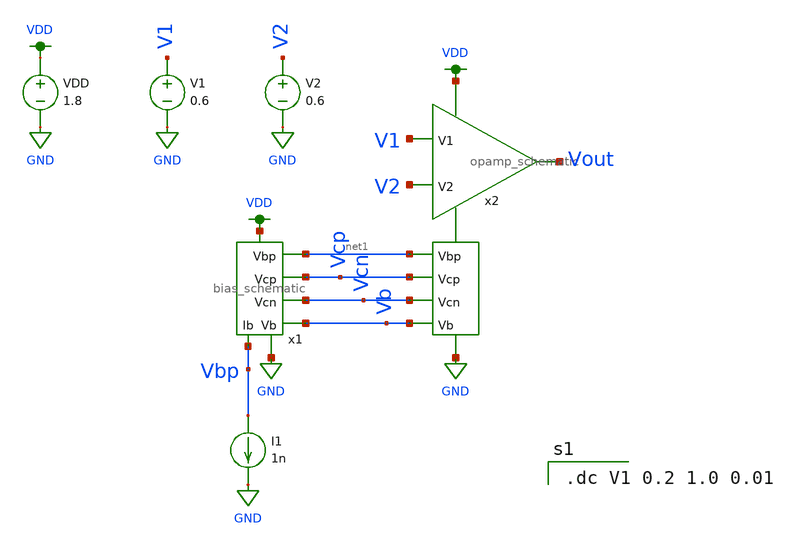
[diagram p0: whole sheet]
** sch_path: mp3/debug_files/test_opamp.sch
**.subckt test_opamp
x1 VDD net1 Vbp Vcp Vcn GND Vb bias_schematic
x2 VDD net1 Vcp Vout V1 V2 Vcn Vb GND opamp_schematic
I1 Vbp GND 1n
V1 V1 GND 0.6
V2 V2 GND 0.6
VDD VDD GND 1.8
**** begin user architecture code

.option wnflag=1
.lib ~/skywater/skywater-pdk/libraries/sky130_fd_pr_ngspice/latest/models/sky130.lib.spice tt


.dc V1 0.2 1.0 0.01

**** end user architecture code
**.ends

* expanding   symbol:  /home/madvlsi/dev/git/vlsi/mp3/xschem/bias_schematic.sym # of pins=7
** sym_path: mp3/debug_files/bias_schematic.sym
** sch_path: mp3/debug_files/bias_schematic.sch
.subckt bias_schematic VP Vbp Ib Vcp Vcn VN Vb
*.iopin VP
*.iopin VN
*.iopin Ib
*.opin Vcp
*.opin Vbp
*.opin Vcn
*.opin Vb
XM1a net2 net2 net1 GND sky130_fd_pr__nfet_01v8 L=0.5 W=30 nf=1 ad='int((nf+1)/2) * W/nf * 0.29' as='int((nf+2)/2) * W/nf * 0.29'
+ pd='2*int((nf+1)/2) * (W/nf + 0.29)' ps='2*int((nf+2)/2) * (W/nf + 0.29)' nrd='0.29 / W' nrs='0.29 / W'
+ sa=0 sb=0 sd=0 mult=1 m=1
XM1b net2 net2 net1 GND sky130_fd_pr__nfet_01v8 L=0.5 W=30 nf=1 ad='int((nf+1)/2) * W/nf * 0.29' as='int((nf+2)/2) * W/nf * 0.29'
+ pd='2*int((nf+1)/2) * (W/nf + 0.29)' ps='2*int((nf+2)/2) * (W/nf + 0.29)' nrd='0.29 / W' nrs='0.29 / W'
+ sa=0 sb=0 sd=0 mult=1 m=1
XM1c net2 net2 net1 GND sky130_fd_pr__nfet_01v8 L=0.5 W=30 nf=1 ad='int((nf+1)/2) * W/nf * 0.29' as='int((nf+2)/2) * W/nf * 0.29'
+ pd='2*int((nf+1)/2) * (W/nf + 0.29)' ps='2*int((nf+2)/2) * (W/nf + 0.29)' nrd='0.29 / W' nrs='0.29 / W'
+ sa=0 sb=0 sd=0 mult=1 m=1
XM1d net2 net2 net1 GND sky130_fd_pr__nfet_01v8 L=0.5 W=30 nf=1 ad='int((nf+1)/2) * W/nf * 0.29' as='int((nf+2)/2) * W/nf * 0.29'
+ pd='2*int((nf+1)/2) * (W/nf + 0.29)' ps='2*int((nf+2)/2) * (W/nf + 0.29)' nrd='0.29 / W' nrs='0.29 / W'
+ sa=0 sb=0 sd=0 mult=1 m=1
XM2a VN net2 net1 GND sky130_fd_pr__nfet_01v8 L=0.5 W=3 nf=1 ad='int((nf+1)/2) * W/nf * 0.29' as='int((nf+2)/2) * W/nf * 0.29'
+ pd='2*int((nf+1)/2) * (W/nf + 0.29)' ps='2*int((nf+2)/2) * (W/nf + 0.29)' nrd='0.29 / W' nrs='0.29 / W'
+ sa=0 sb=0 sd=0 mult=1 m=1
XM2b VN net2 net1 GND sky130_fd_pr__nfet_01v8 L=0.5 W=3 nf=1 ad='int((nf+1)/2) * W/nf * 0.29' as='int((nf+2)/2) * W/nf * 0.29'
+ pd='2*int((nf+1)/2) * (W/nf + 0.29)' ps='2*int((nf+2)/2) * (W/nf + 0.29)' nrd='0.29 / W' nrs='0.29 / W'
+ sa=0 sb=0 sd=0 mult=1 m=1
XM2c VN net2 net1 GND sky130_fd_pr__nfet_01v8 L=0.5 W=3 nf=1 ad='int((nf+1)/2) * W/nf * 0.29' as='int((nf+2)/2) * W/nf * 0.29'
+ pd='2*int((nf+1)/2) * (W/nf + 0.29)' ps='2*int((nf+2)/2) * (W/nf + 0.29)' nrd='0.29 / W' nrs='0.29 / W'
+ sa=0 sb=0 sd=0 mult=1 m=1
XM2d VN net2 net1 GND sky130_fd_pr__nfet_01v8 L=0.5 W=3 nf=1 ad='int((nf+1)/2) * W/nf * 0.29' as='int((nf+2)/2) * W/nf * 0.29'
+ pd='2*int((nf+1)/2) * (W/nf + 0.29)' ps='2*int((nf+2)/2) * (W/nf + 0.29)' nrd='0.29 / W' nrs='0.29 / W'
+ sa=0 sb=0 sd=0 mult=1 m=1
XM3a net2 Ib VP VDD sky130_fd_pr__pfet_01v8 L=0.5 W=3 nf=1 ad='int((nf+1)/2) * W/nf * 0.29' as='int((nf+2)/2) * W/nf * 0.29'
+ pd='2*int((nf+1)/2) * (W/nf + 0.29)' ps='2*int((nf+2)/2) * (W/nf + 0.29)' nrd='0.29 / W' nrs='0.29 / W'
+ sa=0 sb=0 sd=0 mult=1 m=1
XM3b net2 Ib VP VDD sky130_fd_pr__pfet_01v8 L=0.5 W=3 nf=1 ad='int((nf+1)/2) * W/nf * 0.29' as='int((nf+2)/2) * W/nf * 0.29'
+ pd='2*int((nf+1)/2) * (W/nf + 0.29)' ps='2*int((nf+2)/2) * (W/nf + 0.29)' nrd='0.29 / W' nrs='0.29 / W'
+ sa=0 sb=0 sd=0 mult=1 m=1
XM3c net2 Ib VP VDD sky130_fd_pr__pfet_01v8 L=0.5 W=3 nf=1 ad='int((nf+1)/2) * W/nf * 0.29' as='int((nf+2)/2) * W/nf * 0.29'
+ pd='2*int((nf+1)/2) * (W/nf + 0.29)' ps='2*int((nf+2)/2) * (W/nf + 0.29)' nrd='0.29 / W' nrs='0.29 / W'
+ sa=0 sb=0 sd=0 mult=1 m=1
XM3d net2 Ib VP VDD sky130_fd_pr__pfet_01v8 L=0.5 W=3 nf=1 ad='int((nf+1)/2) * W/nf * 0.29' as='int((nf+2)/2) * W/nf * 0.29'
+ pd='2*int((nf+1)/2) * (W/nf + 0.29)' ps='2*int((nf+2)/2) * (W/nf + 0.29)' nrd='0.29 / W' nrs='0.29 / W'
+ sa=0 sb=0 sd=0 mult=1 m=1
XM4a Vcn Ib VP VDD sky130_fd_pr__pfet_01v8 L=0.5 W=30 nf=1 ad='int((nf+1)/2) * W/nf * 0.29' as='int((nf+2)/2) * W/nf * 0.29'
+ pd='2*int((nf+1)/2) * (W/nf + 0.29)' ps='2*int((nf+2)/2) * (W/nf + 0.29)' nrd='0.29 / W' nrs='0.29 / W'
+ sa=0 sb=0 sd=0 mult=1 m=1
XM4b Vcn Ib VP VDD sky130_fd_pr__pfet_01v8 L=0.5 W=30 nf=1 ad='int((nf+1)/2) * W/nf * 0.29' as='int((nf+2)/2) * W/nf * 0.29'
+ pd='2*int((nf+1)/2) * (W/nf + 0.29)' ps='2*int((nf+2)/2) * (W/nf + 0.29)' nrd='0.29 / W' nrs='0.29 / W'
+ sa=0 sb=0 sd=0 mult=1 m=1
XM4c Vcn Ib VP VDD sky130_fd_pr__pfet_01v8 L=0.5 W=30 nf=1 ad='int((nf+1)/2) * W/nf * 0.29' as='int((nf+2)/2) * W/nf * 0.29'
+ pd='2*int((nf+1)/2) * (W/nf + 0.29)' ps='2*int((nf+2)/2) * (W/nf + 0.29)' nrd='0.29 / W' nrs='0.29 / W'
+ sa=0 sb=0 sd=0 mult=1 m=1
XM4d Vcn Ib VP VDD sky130_fd_pr__pfet_01v8 L=0.5 W=30 nf=1 ad='int((nf+1)/2) * W/nf * 0.29' as='int((nf+2)/2) * W/nf * 0.29'
+ pd='2*int((nf+1)/2) * (W/nf + 0.29)' ps='2*int((nf+2)/2) * (W/nf + 0.29)' nrd='0.29 / W' nrs='0.29 / W'
+ sa=0 sb=0 sd=0 mult=1 m=1
XM11a Ib Ib VP VDD sky130_fd_pr__pfet_01v8 L=0.5 W=3 nf=1 ad='int((nf+1)/2) * W/nf * 0.29' as='int((nf+2)/2) * W/nf * 0.29'
+ pd='2*int((nf+1)/2) * (W/nf + 0.29)' ps='2*int((nf+2)/2) * (W/nf + 0.29)' nrd='0.29 / W' nrs='0.29 / W'
+ sa=0 sb=0 sd=0 mult=1 m=1
XM11b Ib Ib VP VDD sky130_fd_pr__pfet_01v8 L=0.5 W=3 nf=1 ad='int((nf+1)/2) * W/nf * 0.29' as='int((nf+2)/2) * W/nf * 0.29'
+ pd='2*int((nf+1)/2) * (W/nf + 0.29)' ps='2*int((nf+2)/2) * (W/nf + 0.29)' nrd='0.29 / W' nrs='0.29 / W'
+ sa=0 sb=0 sd=0 mult=1 m=1
XM11c Ib Ib VP VDD sky130_fd_pr__pfet_01v8 L=0.5 W=3 nf=1 ad='int((nf+1)/2) * W/nf * 0.29' as='int((nf+2)/2) * W/nf * 0.29'
+ pd='2*int((nf+1)/2) * (W/nf + 0.29)' ps='2*int((nf+2)/2) * (W/nf + 0.29)' nrd='0.29 / W' nrs='0.29 / W'
+ sa=0 sb=0 sd=0 mult=1 m=1
XM11d Ib Ib VP VDD sky130_fd_pr__pfet_01v8 L=0.5 W=3 nf=1 ad='int((nf+1)/2) * W/nf * 0.29' as='int((nf+2)/2) * W/nf * 0.29'
+ pd='2*int((nf+1)/2) * (W/nf + 0.29)' ps='2*int((nf+2)/2) * (W/nf + 0.29)' nrd='0.29 / W' nrs='0.29 / W'
+ sa=0 sb=0 sd=0 mult=1 m=1
XM5a net1 Vcn Vcn GND sky130_fd_pr__nfet_01v8 L=0.5 W=30 nf=1 ad='int((nf+1)/2) * W/nf * 0.29' as='int((nf+2)/2) * W/nf * 0.29'
+ pd='2*int((nf+1)/2) * (W/nf + 0.29)' ps='2*int((nf+2)/2) * (W/nf + 0.29)' nrd='0.29 / W' nrs='0.29 / W'
+ sa=0 sb=0 sd=0 mult=1 m=1
XM5b net1 Vcn Vcn GND sky130_fd_pr__nfet_01v8 L=0.5 W=30 nf=1 ad='int((nf+1)/2) * W/nf * 0.29' as='int((nf+2)/2) * W/nf * 0.29'
+ pd='2*int((nf+1)/2) * (W/nf + 0.29)' ps='2*int((nf+2)/2) * (W/nf + 0.29)' nrd='0.29 / W' nrs='0.29 / W'
+ sa=0 sb=0 sd=0 mult=1 m=1
XM5c net1 Vcn Vcn GND sky130_fd_pr__nfet_01v8 L=0.5 W=30 nf=1 ad='int((nf+1)/2) * W/nf * 0.29' as='int((nf+2)/2) * W/nf * 0.29'
+ pd='2*int((nf+1)/2) * (W/nf + 0.29)' ps='2*int((nf+2)/2) * (W/nf + 0.29)' nrd='0.29 / W' nrs='0.29 / W'
+ sa=0 sb=0 sd=0 mult=1 m=1
XM5d net1 Vcn Vcn GND sky130_fd_pr__nfet_01v8 L=0.5 W=30 nf=1 ad='int((nf+1)/2) * W/nf * 0.29' as='int((nf+2)/2) * W/nf * 0.29'
+ pd='2*int((nf+1)/2) * (W/nf + 0.29)' ps='2*int((nf+2)/2) * (W/nf + 0.29)' nrd='0.29 / W' nrs='0.29 / W'
+ sa=0 sb=0 sd=0 mult=1 m=1
XM8a VN Vb net3 GND sky130_fd_pr__nfet_01v8 L=0.5 W=3 nf=1 ad='int((nf+1)/2) * W/nf * 0.29' as='int((nf+2)/2) * W/nf * 0.29'
+ pd='2*int((nf+1)/2) * (W/nf + 0.29)' ps='2*int((nf+2)/2) * (W/nf + 0.29)' nrd='0.29 / W' nrs='0.29 / W'
+ sa=0 sb=0 sd=0 mult=1 m=1
XM8b VN Vb net3 GND sky130_fd_pr__nfet_01v8 L=0.5 W=3 nf=1 ad='int((nf+1)/2) * W/nf * 0.29' as='int((nf+2)/2) * W/nf * 0.29'
+ pd='2*int((nf+1)/2) * (W/nf + 0.29)' ps='2*int((nf+2)/2) * (W/nf + 0.29)' nrd='0.29 / W' nrs='0.29 / W'
+ sa=0 sb=0 sd=0 mult=1 m=1
XM8c VN Vb net3 GND sky130_fd_pr__nfet_01v8 L=0.5 W=3 nf=1 ad='int((nf+1)/2) * W/nf * 0.29' as='int((nf+2)/2) * W/nf * 0.29'
+ pd='2*int((nf+1)/2) * (W/nf + 0.29)' ps='2*int((nf+2)/2) * (W/nf + 0.29)' nrd='0.29 / W' nrs='0.29 / W'
+ sa=0 sb=0 sd=0 mult=1 m=1
XM8d VN Vb net3 GND sky130_fd_pr__nfet_01v8 L=0.5 W=3 nf=1 ad='int((nf+1)/2) * W/nf * 0.29' as='int((nf+2)/2) * W/nf * 0.29'
+ pd='2*int((nf+1)/2) * (W/nf + 0.29)' ps='2*int((nf+2)/2) * (W/nf + 0.29)' nrd='0.29 / W' nrs='0.29 / W'
+ sa=0 sb=0 sd=0 mult=1 m=1
XM6a net3 net3 net4 VDD sky130_fd_pr__pfet_01v8 L=0.5 W=30 nf=1 ad='int((nf+1)/2) * W/nf * 0.29' as='int((nf+2)/2) * W/nf * 0.29'
+ pd='2*int((nf+1)/2) * (W/nf + 0.29)' ps='2*int((nf+2)/2) * (W/nf + 0.29)' nrd='0.29 / W' nrs='0.29 / W'
+ sa=0 sb=0 sd=0 mult=1 m=1
XM6b net3 net3 net4 VDD sky130_fd_pr__pfet_01v8 L=0.5 W=30 nf=1 ad='int((nf+1)/2) * W/nf * 0.29' as='int((nf+2)/2) * W/nf * 0.29'
+ pd='2*int((nf+1)/2) * (W/nf + 0.29)' ps='2*int((nf+2)/2) * (W/nf + 0.29)' nrd='0.29 / W' nrs='0.29 / W'
+ sa=0 sb=0 sd=0 mult=1 m=1
XM6c net3 net3 net4 VDD sky130_fd_pr__pfet_01v8 L=0.5 W=30 nf=1 ad='int((nf+1)/2) * W/nf * 0.29' as='int((nf+2)/2) * W/nf * 0.29'
+ pd='2*int((nf+1)/2) * (W/nf + 0.29)' ps='2*int((nf+2)/2) * (W/nf + 0.29)' nrd='0.29 / W' nrs='0.29 / W'
+ sa=0 sb=0 sd=0 mult=1 m=1
XM6d net3 net3 net4 VDD sky130_fd_pr__pfet_01v8 L=0.5 W=30 nf=1 ad='int((nf+1)/2) * W/nf * 0.29' as='int((nf+2)/2) * W/nf * 0.29'
+ pd='2*int((nf+1)/2) * (W/nf + 0.29)' ps='2*int((nf+2)/2) * (W/nf + 0.29)' nrd='0.29 / W' nrs='0.29 / W'
+ sa=0 sb=0 sd=0 mult=1 m=1
XM7a net4 net3 VP VDD sky130_fd_pr__pfet_01v8 L=0.5 W=3 nf=1 ad='int((nf+1)/2) * W/nf * 0.29' as='int((nf+2)/2) * W/nf * 0.29'
+ pd='2*int((nf+1)/2) * (W/nf + 0.29)' ps='2*int((nf+2)/2) * (W/nf + 0.29)' nrd='0.29 / W' nrs='0.29 / W'
+ sa=0 sb=0 sd=0 mult=1 m=1
XM7b net4 net3 VP VDD sky130_fd_pr__pfet_01v8 L=0.5 W=3 nf=1 ad='int((nf+1)/2) * W/nf * 0.29' as='int((nf+2)/2) * W/nf * 0.29'
+ pd='2*int((nf+1)/2) * (W/nf + 0.29)' ps='2*int((nf+2)/2) * (W/nf + 0.29)' nrd='0.29 / W' nrs='0.29 / W'
+ sa=0 sb=0 sd=0 mult=1 m=1
XM7c net4 net3 VP VDD sky130_fd_pr__pfet_01v8 L=0.5 W=3 nf=1 ad='int((nf+1)/2) * W/nf * 0.29' as='int((nf+2)/2) * W/nf * 0.29'
+ pd='2*int((nf+1)/2) * (W/nf + 0.29)' ps='2*int((nf+2)/2) * (W/nf + 0.29)' nrd='0.29 / W' nrs='0.29 / W'
+ sa=0 sb=0 sd=0 mult=1 m=1
XM7d net4 net3 VP VDD sky130_fd_pr__pfet_01v8 L=0.5 W=3 nf=1 ad='int((nf+1)/2) * W/nf * 0.29' as='int((nf+2)/2) * W/nf * 0.29'
+ pd='2*int((nf+1)/2) * (W/nf + 0.29)' ps='2*int((nf+2)/2) * (W/nf + 0.29)' nrd='0.29 / W' nrs='0.29 / W'
+ sa=0 sb=0 sd=0 mult=1 m=1
XM10d net4 Vcp Vcp VDD sky130_fd_pr__pfet_01v8 L=0.5 W=30 nf=1 ad='int((nf+1)/2) * W/nf * 0.29' as='int((nf+2)/2) * W/nf * 0.29'
+ pd='2*int((nf+1)/2) * (W/nf + 0.29)' ps='2*int((nf+2)/2) * (W/nf + 0.29)' nrd='0.29 / W' nrs='0.29 / W'
+ sa=0 sb=0 sd=0 mult=1 m=1
XM10c net4 Vcp Vcp VDD sky130_fd_pr__pfet_01v8 L=0.5 W=30 nf=1 ad='int((nf+1)/2) * W/nf * 0.29' as='int((nf+2)/2) * W/nf * 0.29'
+ pd='2*int((nf+1)/2) * (W/nf + 0.29)' ps='2*int((nf+2)/2) * (W/nf + 0.29)' nrd='0.29 / W' nrs='0.29 / W'
+ sa=0 sb=0 sd=0 mult=1 m=1
XM10b net4 Vcp Vcp VDD sky130_fd_pr__pfet_01v8 L=0.5 W=30 nf=1 ad='int((nf+1)/2) * W/nf * 0.29' as='int((nf+2)/2) * W/nf * 0.29'
+ pd='2*int((nf+1)/2) * (W/nf + 0.29)' ps='2*int((nf+2)/2) * (W/nf + 0.29)' nrd='0.29 / W' nrs='0.29 / W'
+ sa=0 sb=0 sd=0 mult=1 m=1
XM10a net4 Vcp Vcp VDD sky130_fd_pr__pfet_01v8 L=0.5 W=30 nf=1 ad='int((nf+1)/2) * W/nf * 0.29' as='int((nf+2)/2) * W/nf * 0.29'
+ pd='2*int((nf+1)/2) * (W/nf + 0.29)' ps='2*int((nf+2)/2) * (W/nf + 0.29)' nrd='0.29 / W' nrs='0.29 / W'
+ sa=0 sb=0 sd=0 mult=1 m=1
XM9a VN Vb Vcp GND sky130_fd_pr__nfet_01v8 L=0.5 W=30 nf=1 ad='int((nf+1)/2) * W/nf * 0.29' as='int((nf+2)/2) * W/nf * 0.29'
+ pd='2*int((nf+1)/2) * (W/nf + 0.29)' ps='2*int((nf+2)/2) * (W/nf + 0.29)' nrd='0.29 / W' nrs='0.29 / W'
+ sa=0 sb=0 sd=0 mult=1 m=1
XM9b VN Vb Vcp GND sky130_fd_pr__nfet_01v8 L=0.5 W=30 nf=1 ad='int((nf+1)/2) * W/nf * 0.29' as='int((nf+2)/2) * W/nf * 0.29'
+ pd='2*int((nf+1)/2) * (W/nf + 0.29)' ps='2*int((nf+2)/2) * (W/nf + 0.29)' nrd='0.29 / W' nrs='0.29 / W'
+ sa=0 sb=0 sd=0 mult=1 m=1
XM9c VN Vb Vcp GND sky130_fd_pr__nfet_01v8 L=0.5 W=30 nf=1 ad='int((nf+1)/2) * W/nf * 0.29' as='int((nf+2)/2) * W/nf * 0.29'
+ pd='2*int((nf+1)/2) * (W/nf + 0.29)' ps='2*int((nf+2)/2) * (W/nf + 0.29)' nrd='0.29 / W' nrs='0.29 / W'
+ sa=0 sb=0 sd=0 mult=1 m=1
XM9d VN Vb Vcp GND sky130_fd_pr__nfet_01v8 L=0.5 W=30 nf=1 ad='int((nf+1)/2) * W/nf * 0.29' as='int((nf+2)/2) * W/nf * 0.29'
+ pd='2*int((nf+1)/2) * (W/nf + 0.29)' ps='2*int((nf+2)/2) * (W/nf + 0.29)' nrd='0.29 / W' nrs='0.29 / W'
+ sa=0 sb=0 sd=0 mult=1 m=1
XM12a VN Vb Vb GND sky130_fd_pr__nfet_01v8 L=0.5 W=3 nf=1 ad='int((nf+1)/2) * W/nf * 0.29' as='int((nf+2)/2) * W/nf * 0.29'
+ pd='2*int((nf+1)/2) * (W/nf + 0.29)' ps='2*int((nf+2)/2) * (W/nf + 0.29)' nrd='0.29 / W' nrs='0.29 / W'
+ sa=0 sb=0 sd=0 mult=1 m=1
XM12b VN Vb Vb GND sky130_fd_pr__nfet_01v8 L=0.5 W=3 nf=1 ad='int((nf+1)/2) * W/nf * 0.29' as='int((nf+2)/2) * W/nf * 0.29'
+ pd='2*int((nf+1)/2) * (W/nf + 0.29)' ps='2*int((nf+2)/2) * (W/nf + 0.29)' nrd='0.29 / W' nrs='0.29 / W'
+ sa=0 sb=0 sd=0 mult=1 m=1
XM12c VN Vb Vb GND sky130_fd_pr__nfet_01v8 L=0.5 W=3 nf=1 ad='int((nf+1)/2) * W/nf * 0.29' as='int((nf+2)/2) * W/nf * 0.29'
+ pd='2*int((nf+1)/2) * (W/nf + 0.29)' ps='2*int((nf+2)/2) * (W/nf + 0.29)' nrd='0.29 / W' nrs='0.29 / W'
+ sa=0 sb=0 sd=0 mult=1 m=1
XM12d VN Vb Vb GND sky130_fd_pr__nfet_01v8 L=0.5 W=3 nf=1 ad='int((nf+1)/2) * W/nf * 0.29' as='int((nf+2)/2) * W/nf * 0.29'
+ pd='2*int((nf+1)/2) * (W/nf + 0.29)' ps='2*int((nf+2)/2) * (W/nf + 0.29)' nrd='0.29 / W' nrs='0.29 / W'
+ sa=0 sb=0 sd=0 mult=1 m=1
XM1 Vb Ib VP VDD sky130_fd_pr__pfet_01v8 L=0.5 W=3 nf=1 ad='int((nf+1)/2) * W/nf * 0.29' as='int((nf+2)/2) * W/nf * 0.29'
+ pd='2*int((nf+1)/2) * (W/nf + 0.29)' ps='2*int((nf+2)/2) * (W/nf + 0.29)' nrd='0.29 / W' nrs='0.29 / W'
+ sa=0 sb=0 sd=0 mult=1 m=1
XM2 Vb Ib VP VDD sky130_fd_pr__pfet_01v8 L=0.5 W=3 nf=1 ad='int((nf+1)/2) * W/nf * 0.29' as='int((nf+2)/2) * W/nf * 0.29'
+ pd='2*int((nf+1)/2) * (W/nf + 0.29)' ps='2*int((nf+2)/2) * (W/nf + 0.29)' nrd='0.29 / W' nrs='0.29 / W'
+ sa=0 sb=0 sd=0 mult=1 m=1
XM3 Vb Ib VP VDD sky130_fd_pr__pfet_01v8 L=0.5 W=3 nf=1 ad='int((nf+1)/2) * W/nf * 0.29' as='int((nf+2)/2) * W/nf * 0.29'
+ pd='2*int((nf+1)/2) * (W/nf + 0.29)' ps='2*int((nf+2)/2) * (W/nf + 0.29)' nrd='0.29 / W' nrs='0.29 / W'
+ sa=0 sb=0 sd=0 mult=1 m=1
XM4 Vb Ib VP VDD sky130_fd_pr__pfet_01v8 L=0.5 W=3 nf=1 ad='int((nf+1)/2) * W/nf * 0.29' as='int((nf+2)/2) * W/nf * 0.29'
+ pd='2*int((nf+1)/2) * (W/nf + 0.29)' ps='2*int((nf+2)/2) * (W/nf + 0.29)' nrd='0.29 / W' nrs='0.29 / W'
+ sa=0 sb=0 sd=0 mult=1 m=1
.ends


* expanding   symbol:  /home/madvlsi/dev/git/vlsi/mp3/xschem/opamp_schematic.sym # of pins=9
** sym_path: /home/madvlsi/dev/git/vlsi/mp3/xschem/opamp_schematic.sym
** sch_path: /home/madvlsi/dev/git/vlsi/mp3/xschem/opamp_schematic.sch
.subckt opamp_schematic VP Vbp Vcp Vout V1 V2 Vcn Vb VN
*.ipin Vbp
*.ipin Vcp
*.ipin Vcn
*.ipin V2
*.ipin V1
*.ipin Vb
*.iopin VP
*.iopin VN
*.opin Vout
XM1a M1top V1 Vnode GND sky130_fd_pr__nfet_01v8 L=0.5 W=3 nf=1 ad='int((nf+1)/2) * W/nf * 0.29' as='int((nf+2)/2) * W/nf * 0.29'
+ pd='2*int((nf+1)/2) * (W/nf + 0.29)' ps='2*int((nf+2)/2) * (W/nf + 0.29)' nrd='0.29 / W' nrs='0.29 / W'
+ sa=0 sb=0 sd=0 mult=1 m=1
XM1b M1top V1 Vnode GND sky130_fd_pr__nfet_01v8 L=0.5 W=3 nf=1 ad='int((nf+1)/2) * W/nf * 0.29' as='int((nf+2)/2) * W/nf * 0.29'
+ pd='2*int((nf+1)/2) * (W/nf + 0.29)' ps='2*int((nf+2)/2) * (W/nf + 0.29)' nrd='0.29 / W' nrs='0.29 / W'
+ sa=0 sb=0 sd=0 mult=1 m=1
XM1c M1top V1 Vnode GND sky130_fd_pr__nfet_01v8 L=0.5 W=3 nf=1 ad='int((nf+1)/2) * W/nf * 0.29' as='int((nf+2)/2) * W/nf * 0.29'
+ pd='2*int((nf+1)/2) * (W/nf + 0.29)' ps='2*int((nf+2)/2) * (W/nf + 0.29)' nrd='0.29 / W' nrs='0.29 / W'
+ sa=0 sb=0 sd=0 mult=1 m=1
XM1d M1top V1 Vnode GND sky130_fd_pr__nfet_01v8 L=0.5 W=3 nf=1 ad='int((nf+1)/2) * W/nf * 0.29' as='int((nf+2)/2) * W/nf * 0.29'
+ pd='2*int((nf+1)/2) * (W/nf + 0.29)' ps='2*int((nf+2)/2) * (W/nf + 0.29)' nrd='0.29 / W' nrs='0.29 / W'
+ sa=0 sb=0 sd=0 mult=1 m=1
XM2a M2top V2 Vnode GND sky130_fd_pr__nfet_01v8 L=0.5 W=3 nf=1 ad='int((nf+1)/2) * W/nf * 0.29' as='int((nf+2)/2) * W/nf * 0.29'
+ pd='2*int((nf+1)/2) * (W/nf + 0.29)' ps='2*int((nf+2)/2) * (W/nf + 0.29)' nrd='0.29 / W' nrs='0.29 / W'
+ sa=0 sb=0 sd=0 mult=1 m=1
XM2b M2top V2 Vnode GND sky130_fd_pr__nfet_01v8 L=0.5 W=3 nf=1 ad='int((nf+1)/2) * W/nf * 0.29' as='int((nf+2)/2) * W/nf * 0.29'
+ pd='2*int((nf+1)/2) * (W/nf + 0.29)' ps='2*int((nf+2)/2) * (W/nf + 0.29)' nrd='0.29 / W' nrs='0.29 / W'
+ sa=0 sb=0 sd=0 mult=1 m=1
XM2c M2top V2 Vnode GND sky130_fd_pr__nfet_01v8 L=0.5 W=3 nf=1 ad='int((nf+1)/2) * W/nf * 0.29' as='int((nf+2)/2) * W/nf * 0.29'
+ pd='2*int((nf+1)/2) * (W/nf + 0.29)' ps='2*int((nf+2)/2) * (W/nf + 0.29)' nrd='0.29 / W' nrs='0.29 / W'
+ sa=0 sb=0 sd=0 mult=1 m=1
XM2d M2top V2 Vnode GND sky130_fd_pr__nfet_01v8 L=0.5 W=3 nf=1 ad='int((nf+1)/2) * W/nf * 0.29' as='int((nf+2)/2) * W/nf * 0.29'
+ pd='2*int((nf+1)/2) * (W/nf + 0.29)' ps='2*int((nf+2)/2) * (W/nf + 0.29)' nrd='0.29 / W' nrs='0.29 / W'
+ sa=0 sb=0 sd=0 mult=1 m=1
XMba Vnode Vb VN GND sky130_fd_pr__nfet_01v8 L=0.5 W=1.5 nf=1 ad='int((nf+1)/2) * W/nf * 0.29' as='int((nf+2)/2) * W/nf * 0.29'
+ pd='2*int((nf+1)/2) * (W/nf + 0.29)' ps='2*int((nf+2)/2) * (W/nf + 0.29)' nrd='0.29 / W' nrs='0.29 / W'
+ sa=0 sb=0 sd=0 mult=1 m=1
XMbb Vnode Vb VN GND sky130_fd_pr__nfet_01v8 L=0.5 W=1.5 nf=1 ad='int((nf+1)/2) * W/nf * 0.29' as='int((nf+2)/2) * W/nf * 0.29'
+ pd='2*int((nf+1)/2) * (W/nf + 0.29)' ps='2*int((nf+2)/2) * (W/nf + 0.29)' nrd='0.29 / W' nrs='0.29 / W'
+ sa=0 sb=0 sd=0 mult=1 m=1
XMbc Vnode Vb VN GND sky130_fd_pr__nfet_01v8 L=0.5 W=1.5 nf=1 ad='int((nf+1)/2) * W/nf * 0.29' as='int((nf+2)/2) * W/nf * 0.29'
+ pd='2*int((nf+1)/2) * (W/nf + 0.29)' ps='2*int((nf+2)/2) * (W/nf + 0.29)' nrd='0.29 / W' nrs='0.29 / W'
+ sa=0 sb=0 sd=0 mult=1 m=1
XMbd Vnode Vb VN GND sky130_fd_pr__nfet_01v8 L=0.5 W=1.5 nf=1 ad='int((nf+1)/2) * W/nf * 0.29' as='int((nf+2)/2) * W/nf * 0.29'
+ pd='2*int((nf+1)/2) * (W/nf + 0.29)' ps='2*int((nf+2)/2) * (W/nf + 0.29)' nrd='0.29 / W' nrs='0.29 / W'
+ sa=0 sb=0 sd=0 mult=1 m=1
XMbe Vnode Vb VN GND sky130_fd_pr__nfet_01v8 L=0.5 W=1.5 nf=1 ad='int((nf+1)/2) * W/nf * 0.29' as='int((nf+2)/2) * W/nf * 0.29'
+ pd='2*int((nf+1)/2) * (W/nf + 0.29)' ps='2*int((nf+2)/2) * (W/nf + 0.29)' nrd='0.29 / W' nrs='0.29 / W'
+ sa=0 sb=0 sd=0 mult=1 m=1
XMbf Vnode Vb VN GND sky130_fd_pr__nfet_01v8 L=0.5 W=1.5 nf=1 ad='int((nf+1)/2) * W/nf * 0.29' as='int((nf+2)/2) * W/nf * 0.29'
+ pd='2*int((nf+1)/2) * (W/nf + 0.29)' ps='2*int((nf+2)/2) * (W/nf + 0.29)' nrd='0.29 / W' nrs='0.29 / W'
+ sa=0 sb=0 sd=0 mult=1 m=1
XMbg Vnode Vb VN GND sky130_fd_pr__nfet_01v8 L=0.5 W=1.5 nf=1 ad='int((nf+1)/2) * W/nf * 0.29' as='int((nf+2)/2) * W/nf * 0.29'
+ pd='2*int((nf+1)/2) * (W/nf + 0.29)' ps='2*int((nf+2)/2) * (W/nf + 0.29)' nrd='0.29 / W' nrs='0.29 / W'
+ sa=0 sb=0 sd=0 mult=1 m=1
XMbh Vnode Vb VN GND sky130_fd_pr__nfet_01v8 L=0.5 W=1.5 nf=1 ad='int((nf+1)/2) * W/nf * 0.29' as='int((nf+2)/2) * W/nf * 0.29'
+ pd='2*int((nf+1)/2) * (W/nf + 0.29)' ps='2*int((nf+2)/2) * (W/nf + 0.29)' nrd='0.29 / W' nrs='0.29 / W'
+ sa=0 sb=0 sd=0 mult=1 m=1
XM7a net2 Vcn net1 GND sky130_fd_pr__nfet_01v8 L=0.5 W=3 nf=1 ad='int((nf+1)/2) * W/nf * 0.29' as='int((nf+2)/2) * W/nf * 0.29'
+ pd='2*int((nf+1)/2) * (W/nf + 0.29)' ps='2*int((nf+2)/2) * (W/nf + 0.29)' nrd='0.29 / W' nrs='0.29 / W'
+ sa=0 sb=0 sd=0 mult=1 m=1
XM7b net2 Vcn net1 GND sky130_fd_pr__nfet_01v8 L=0.5 W=3 nf=1 ad='int((nf+1)/2) * W/nf * 0.29' as='int((nf+2)/2) * W/nf * 0.29'
+ pd='2*int((nf+1)/2) * (W/nf + 0.29)' ps='2*int((nf+2)/2) * (W/nf + 0.29)' nrd='0.29 / W' nrs='0.29 / W'
+ sa=0 sb=0 sd=0 mult=1 m=1
XM7c net2 Vcn net1 GND sky130_fd_pr__nfet_01v8 L=0.5 W=3 nf=1 ad='int((nf+1)/2) * W/nf * 0.29' as='int((nf+2)/2) * W/nf * 0.29'
+ pd='2*int((nf+1)/2) * (W/nf + 0.29)' ps='2*int((nf+2)/2) * (W/nf + 0.29)' nrd='0.29 / W' nrs='0.29 / W'
+ sa=0 sb=0 sd=0 mult=1 m=1
XM7d net2 Vcn net1 GND sky130_fd_pr__nfet_01v8 L=0.5 W=3 nf=1 ad='int((nf+1)/2) * W/nf * 0.29' as='int((nf+2)/2) * W/nf * 0.29'
+ pd='2*int((nf+1)/2) * (W/nf + 0.29)' ps='2*int((nf+2)/2) * (W/nf + 0.29)' nrd='0.29 / W' nrs='0.29 / W'
+ sa=0 sb=0 sd=0 mult=1 m=1
XM8a net3 Vcn Vout GND sky130_fd_pr__nfet_01v8 L=0.5 W=3 nf=1 ad='int((nf+1)/2) * W/nf * 0.29' as='int((nf+2)/2) * W/nf * 0.29'
+ pd='2*int((nf+1)/2) * (W/nf + 0.29)' ps='2*int((nf+2)/2) * (W/nf + 0.29)' nrd='0.29 / W' nrs='0.29 / W'
+ sa=0 sb=0 sd=0 mult=1 m=1
XM8b net3 Vcn Vout GND sky130_fd_pr__nfet_01v8 L=0.5 W=3 nf=1 ad='int((nf+1)/2) * W/nf * 0.29' as='int((nf+2)/2) * W/nf * 0.29'
+ pd='2*int((nf+1)/2) * (W/nf + 0.29)' ps='2*int((nf+2)/2) * (W/nf + 0.29)' nrd='0.29 / W' nrs='0.29 / W'
+ sa=0 sb=0 sd=0 mult=1 m=1
XM8c net3 Vcn Vout GND sky130_fd_pr__nfet_01v8 L=0.5 W=3 nf=1 ad='int((nf+1)/2) * W/nf * 0.29' as='int((nf+2)/2) * W/nf * 0.29'
+ pd='2*int((nf+1)/2) * (W/nf + 0.29)' ps='2*int((nf+2)/2) * (W/nf + 0.29)' nrd='0.29 / W' nrs='0.29 / W'
+ sa=0 sb=0 sd=0 mult=1 m=1
XM8d net3 Vcn Vout GND sky130_fd_pr__nfet_01v8 L=0.5 W=3 nf=1 ad='int((nf+1)/2) * W/nf * 0.29' as='int((nf+2)/2) * W/nf * 0.29'
+ pd='2*int((nf+1)/2) * (W/nf + 0.29)' ps='2*int((nf+2)/2) * (W/nf + 0.29)' nrd='0.29 / W' nrs='0.29 / W'
+ sa=0 sb=0 sd=0 mult=1 m=1
XM9a net1 net2 VN GND sky130_fd_pr__nfet_01v8 L=0.5 W=3 nf=1 ad='int((nf+1)/2) * W/nf * 0.29' as='int((nf+2)/2) * W/nf * 0.29'
+ pd='2*int((nf+1)/2) * (W/nf + 0.29)' ps='2*int((nf+2)/2) * (W/nf + 0.29)' nrd='0.29 / W' nrs='0.29 / W'
+ sa=0 sb=0 sd=0 mult=1 m=1
XM9b net1 net2 VN GND sky130_fd_pr__nfet_01v8 L=0.5 W=3 nf=1 ad='int((nf+1)/2) * W/nf * 0.29' as='int((nf+2)/2) * W/nf * 0.29'
+ pd='2*int((nf+1)/2) * (W/nf + 0.29)' ps='2*int((nf+2)/2) * (W/nf + 0.29)' nrd='0.29 / W' nrs='0.29 / W'
+ sa=0 sb=0 sd=0 mult=1 m=1
XM9c net1 net2 VN GND sky130_fd_pr__nfet_01v8 L=0.5 W=3 nf=1 ad='int((nf+1)/2) * W/nf * 0.29' as='int((nf+2)/2) * W/nf * 0.29'
+ pd='2*int((nf+1)/2) * (W/nf + 0.29)' ps='2*int((nf+2)/2) * (W/nf + 0.29)' nrd='0.29 / W' nrs='0.29 / W'
+ sa=0 sb=0 sd=0 mult=1 m=1
XM9d net1 net2 VN GND sky130_fd_pr__nfet_01v8 L=0.5 W=3 nf=1 ad='int((nf+1)/2) * W/nf * 0.29' as='int((nf+2)/2) * W/nf * 0.29'
+ pd='2*int((nf+1)/2) * (W/nf + 0.29)' ps='2*int((nf+2)/2) * (W/nf + 0.29)' nrd='0.29 / W' nrs='0.29 / W'
+ sa=0 sb=0 sd=0 mult=1 m=1
XM10a VN net2 net3 GND sky130_fd_pr__nfet_01v8 L=0.5 W=3 nf=1 ad='int((nf+1)/2) * W/nf * 0.29' as='int((nf+2)/2) * W/nf * 0.29'
+ pd='2*int((nf+1)/2) * (W/nf + 0.29)' ps='2*int((nf+2)/2) * (W/nf + 0.29)' nrd='0.29 / W' nrs='0.29 / W'
+ sa=0 sb=0 sd=0 mult=1 m=1
XM10b VN net2 net3 GND sky130_fd_pr__nfet_01v8 L=0.5 W=3 nf=1 ad='int((nf+1)/2) * W/nf * 0.29' as='int((nf+2)/2) * W/nf * 0.29'
+ pd='2*int((nf+1)/2) * (W/nf + 0.29)' ps='2*int((nf+2)/2) * (W/nf + 0.29)' nrd='0.29 / W' nrs='0.29 / W'
+ sa=0 sb=0 sd=0 mult=1 m=1
XM10c VN net2 net3 GND sky130_fd_pr__nfet_01v8 L=0.5 W=3 nf=1 ad='int((nf+1)/2) * W/nf * 0.29' as='int((nf+2)/2) * W/nf * 0.29'
+ pd='2*int((nf+1)/2) * (W/nf + 0.29)' ps='2*int((nf+2)/2) * (W/nf + 0.29)' nrd='0.29 / W' nrs='0.29 / W'
+ sa=0 sb=0 sd=0 mult=1 m=1
XM1 VN net2 net3 GND sky130_fd_pr__nfet_01v8 L=0.5 W=3 nf=1 ad='int((nf+1)/2) * W/nf * 0.29' as='int((nf+2)/2) * W/nf * 0.29'
+ pd='2*int((nf+1)/2) * (W/nf + 0.29)' ps='2*int((nf+2)/2) * (W/nf + 0.29)' nrd='0.29 / W' nrs='0.29 / W'
+ sa=0 sb=0 sd=0 mult=1 m=1
XM5a net2 Vcp M1top VDD sky130_fd_pr__pfet_01v8 L=0.5 W=3 nf=1 ad='int((nf+1)/2) * W/nf * 0.29' as='int((nf+2)/2) * W/nf * 0.29'
+ pd='2*int((nf+1)/2) * (W/nf + 0.29)' ps='2*int((nf+2)/2) * (W/nf + 0.29)' nrd='0.29 / W' nrs='0.29 / W'
+ sa=0 sb=0 sd=0 mult=1 m=1
XM5b net2 Vcp M1top VDD sky130_fd_pr__pfet_01v8 L=0.5 W=3 nf=1 ad='int((nf+1)/2) * W/nf * 0.29' as='int((nf+2)/2) * W/nf * 0.29'
+ pd='2*int((nf+1)/2) * (W/nf + 0.29)' ps='2*int((nf+2)/2) * (W/nf + 0.29)' nrd='0.29 / W' nrs='0.29 / W'
+ sa=0 sb=0 sd=0 mult=1 m=1
XM5c net2 Vcp M1top VDD sky130_fd_pr__pfet_01v8 L=0.5 W=3 nf=1 ad='int((nf+1)/2) * W/nf * 0.29' as='int((nf+2)/2) * W/nf * 0.29'
+ pd='2*int((nf+1)/2) * (W/nf + 0.29)' ps='2*int((nf+2)/2) * (W/nf + 0.29)' nrd='0.29 / W' nrs='0.29 / W'
+ sa=0 sb=0 sd=0 mult=1 m=1
XM5d net2 Vcp M1top VDD sky130_fd_pr__pfet_01v8 L=0.5 W=3 nf=1 ad='int((nf+1)/2) * W/nf * 0.29' as='int((nf+2)/2) * W/nf * 0.29'
+ pd='2*int((nf+1)/2) * (W/nf + 0.29)' ps='2*int((nf+2)/2) * (W/nf + 0.29)' nrd='0.29 / W' nrs='0.29 / W'
+ sa=0 sb=0 sd=0 mult=1 m=1
XM6a Vout Vcp M2top VDD sky130_fd_pr__pfet_01v8 L=0.5 W=3 nf=1 ad='int((nf+1)/2) * W/nf * 0.29' as='int((nf+2)/2) * W/nf * 0.29'
+ pd='2*int((nf+1)/2) * (W/nf + 0.29)' ps='2*int((nf+2)/2) * (W/nf + 0.29)' nrd='0.29 / W' nrs='0.29 / W'
+ sa=0 sb=0 sd=0 mult=1 m=1
XM6b Vout Vcp M2top VDD sky130_fd_pr__pfet_01v8 L=0.5 W=3 nf=1 ad='int((nf+1)/2) * W/nf * 0.29' as='int((nf+2)/2) * W/nf * 0.29'
+ pd='2*int((nf+1)/2) * (W/nf + 0.29)' ps='2*int((nf+2)/2) * (W/nf + 0.29)' nrd='0.29 / W' nrs='0.29 / W'
+ sa=0 sb=0 sd=0 mult=1 m=1
XM6c Vout Vcp M2top VDD sky130_fd_pr__pfet_01v8 L=0.5 W=3 nf=1 ad='int((nf+1)/2) * W/nf * 0.29' as='int((nf+2)/2) * W/nf * 0.29'
+ pd='2*int((nf+1)/2) * (W/nf + 0.29)' ps='2*int((nf+2)/2) * (W/nf + 0.29)' nrd='0.29 / W' nrs='0.29 / W'
+ sa=0 sb=0 sd=0 mult=1 m=1
XM6d Vout Vcp M2top VDD sky130_fd_pr__pfet_01v8 L=0.5 W=3 nf=1 ad='int((nf+1)/2) * W/nf * 0.29' as='int((nf+2)/2) * W/nf * 0.29'
+ pd='2*int((nf+1)/2) * (W/nf + 0.29)' ps='2*int((nf+2)/2) * (W/nf + 0.29)' nrd='0.29 / W' nrs='0.29 / W'
+ sa=0 sb=0 sd=0 mult=1 m=1
XM3a M1top Vbp VP VDD sky130_fd_pr__pfet_01v8 L=0.5 W=3 nf=1 ad='int((nf+1)/2) * W/nf * 0.29' as='int((nf+2)/2) * W/nf * 0.29'
+ pd='2*int((nf+1)/2) * (W/nf + 0.29)' ps='2*int((nf+2)/2) * (W/nf + 0.29)' nrd='0.29 / W' nrs='0.29 / W'
+ sa=0 sb=0 sd=0 mult=1 m=1
XM3b M1top Vbp VP VDD sky130_fd_pr__pfet_01v8 L=0.5 W=3 nf=1 ad='int((nf+1)/2) * W/nf * 0.29' as='int((nf+2)/2) * W/nf * 0.29'
+ pd='2*int((nf+1)/2) * (W/nf + 0.29)' ps='2*int((nf+2)/2) * (W/nf + 0.29)' nrd='0.29 / W' nrs='0.29 / W'
+ sa=0 sb=0 sd=0 mult=1 m=1
XM3c M1top Vbp VP VDD sky130_fd_pr__pfet_01v8 L=0.5 W=3 nf=1 ad='int((nf+1)/2) * W/nf * 0.29' as='int((nf+2)/2) * W/nf * 0.29'
+ pd='2*int((nf+1)/2) * (W/nf + 0.29)' ps='2*int((nf+2)/2) * (W/nf + 0.29)' nrd='0.29 / W' nrs='0.29 / W'
+ sa=0 sb=0 sd=0 mult=1 m=1
XM3d M1top Vbp VP VDD sky130_fd_pr__pfet_01v8 L=0.5 W=3 nf=1 ad='int((nf+1)/2) * W/nf * 0.29' as='int((nf+2)/2) * W/nf * 0.29'
+ pd='2*int((nf+1)/2) * (W/nf + 0.29)' ps='2*int((nf+2)/2) * (W/nf + 0.29)' nrd='0.29 / W' nrs='0.29 / W'
+ sa=0 sb=0 sd=0 mult=1 m=1
XM4a M2top Vbp VP VDD sky130_fd_pr__pfet_01v8 L=0.5 W=3 nf=1 ad='int((nf+1)/2) * W/nf * 0.29' as='int((nf+2)/2) * W/nf * 0.29'
+ pd='2*int((nf+1)/2) * (W/nf + 0.29)' ps='2*int((nf+2)/2) * (W/nf + 0.29)' nrd='0.29 / W' nrs='0.29 / W'
+ sa=0 sb=0 sd=0 mult=1 m=1
XM4b M2top Vbp VP VDD sky130_fd_pr__pfet_01v8 L=0.5 W=3 nf=1 ad='int((nf+1)/2) * W/nf * 0.29' as='int((nf+2)/2) * W/nf * 0.29'
+ pd='2*int((nf+1)/2) * (W/nf + 0.29)' ps='2*int((nf+2)/2) * (W/nf + 0.29)' nrd='0.29 / W' nrs='0.29 / W'
+ sa=0 sb=0 sd=0 mult=1 m=1
XM4c M2top Vbp VP VDD sky130_fd_pr__pfet_01v8 L=0.5 W=3 nf=1 ad='int((nf+1)/2) * W/nf * 0.29' as='int((nf+2)/2) * W/nf * 0.29'
+ pd='2*int((nf+1)/2) * (W/nf + 0.29)' ps='2*int((nf+2)/2) * (W/nf + 0.29)' nrd='0.29 / W' nrs='0.29 / W'
+ sa=0 sb=0 sd=0 mult=1 m=1
XM4d M2top Vbp VP VDD sky130_fd_pr__pfet_01v8 L=0.5 W=3 nf=1 ad='int((nf+1)/2) * W/nf * 0.29' as='int((nf+2)/2) * W/nf * 0.29'
+ pd='2*int((nf+1)/2) * (W/nf + 0.29)' ps='2*int((nf+2)/2) * (W/nf + 0.29)' nrd='0.29 / W' nrs='0.29 / W'
+ sa=0 sb=0 sd=0 mult=1 m=1
.ends

.GLOBAL VDD
.GLOBAL GND
.end
